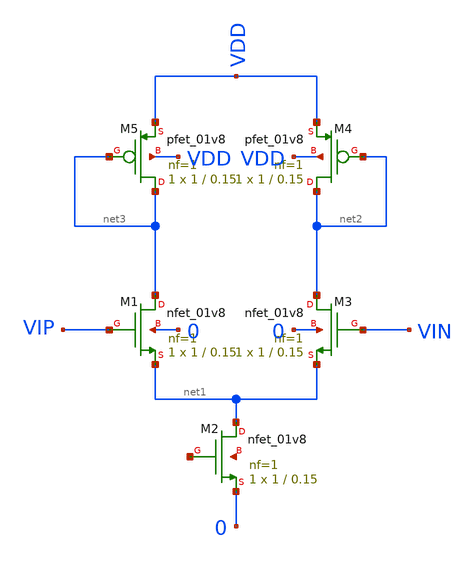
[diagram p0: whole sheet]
** sch_path: untitled.sch
**.subckt untitled
XM1 net3 VIP net1 0 sky130_fd_pr__nfet_01v8 L=0.15 W=1 nf=1 ad='int((nf+1)/2) * W/nf * 0.29' as='int((nf+2)/2) * W/nf * 0.29'
+ pd='2*int((nf+1)/2) * (W/nf + 0.29)' ps='2*int((nf+2)/2) * (W/nf + 0.29)' nrd='0.29 / W' nrs='0.29 / W'
+ sa=0 sb=0 sd=0 mult=1 m=1
XM2 net1 net4 0 net5 sky130_fd_pr__nfet_01v8 L=0.15 W=1 nf=1 ad='int((nf+1)/2) * W/nf * 0.29' as='int((nf+2)/2) * W/nf * 0.29'
+ pd='2*int((nf+1)/2) * (W/nf + 0.29)' ps='2*int((nf+2)/2) * (W/nf + 0.29)' nrd='0.29 / W' nrs='0.29 / W'
+ sa=0 sb=0 sd=0 mult=1 m=1
XM3 net2 VIN net1 0 sky130_fd_pr__nfet_01v8 L=0.15 W=1 nf=1 ad='int((nf+1)/2) * W/nf * 0.29' as='int((nf+2)/2) * W/nf * 0.29'
+ pd='2*int((nf+1)/2) * (W/nf + 0.29)' ps='2*int((nf+2)/2) * (W/nf + 0.29)' nrd='0.29 / W' nrs='0.29 / W'
+ sa=0 sb=0 sd=0 mult=1 m=1
XM4 net2 net2 VDD VDD sky130_fd_pr__pfet_01v8 L=0.15 W=1 nf=1 ad='int((nf+1)/2) * W/nf * 0.29' as='int((nf+2)/2) * W/nf * 0.29'
+ pd='2*int((nf+1)/2) * (W/nf + 0.29)' ps='2*int((nf+2)/2) * (W/nf + 0.29)' nrd='0.29 / W' nrs='0.29 / W'
+ sa=0 sb=0 sd=0 mult=1 m=1
XM5 net3 net3 VDD VDD sky130_fd_pr__pfet_01v8 L=0.15 W=1 nf=1 ad='int((nf+1)/2) * W/nf * 0.29' as='int((nf+2)/2) * W/nf * 0.29'
+ pd='2*int((nf+1)/2) * (W/nf + 0.29)' ps='2*int((nf+2)/2) * (W/nf + 0.29)' nrd='0.29 / W' nrs='0.29 / W'
+ sa=0 sb=0 sd=0 mult=1 m=1
**.ends
.end
